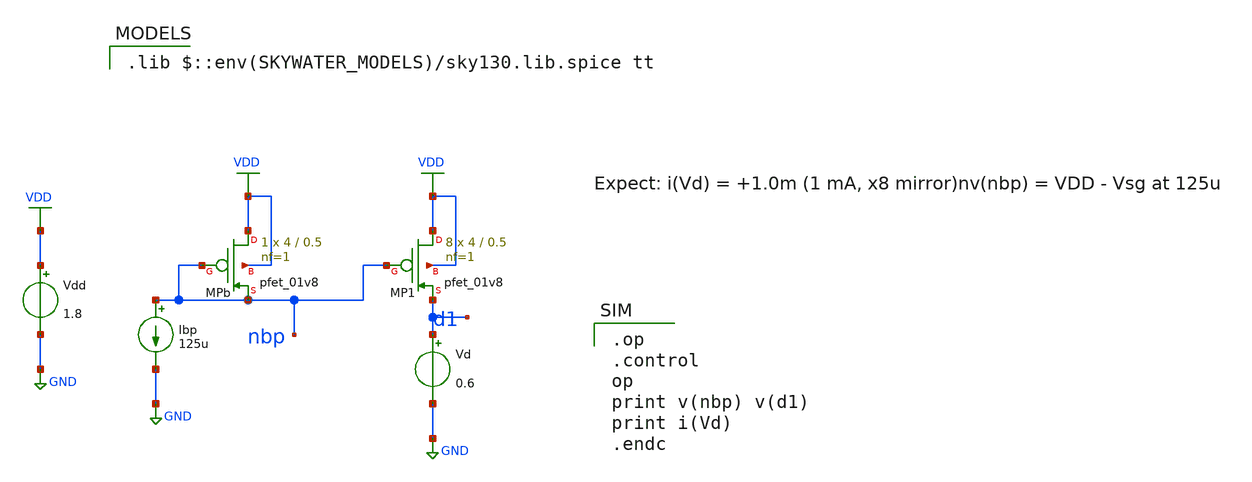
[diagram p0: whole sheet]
** sch_path: 09-sky130-gilbert-mixer-rfic/schematics/2_bleed_bias.sch
**.subckt 2_bleed_bias
XMPb VDD nbp nbp VDD sky130_fd_pr__pfet_01v8 L=0.5 W=4 nf=1 ad='int((nf+1)/2) * W/nf * 0.29' as='int((nf+2)/2) * W/nf * 0.29'
+ pd='2*int((nf+1)/2) * (W/nf + 0.29)' ps='2*int((nf+2)/2) * (W/nf + 0.29)' nrd='0.29 / W' nrs='0.29 / W'
+ sa=0 sb=0 sd=0 mult=1 m=1
Ibp nbp GND 125u
XMP1 VDD nbp d1 VDD sky130_fd_pr__pfet_01v8 L=0.5 W=4 nf=1 ad='int((nf+1)/2) * W/nf * 0.29' as='int((nf+2)/2) * W/nf * 0.29'
+ pd='2*int((nf+1)/2) * (W/nf + 0.29)' ps='2*int((nf+2)/2) * (W/nf + 0.29)' nrd='0.29 / W' nrs='0.29 / W'
+ sa=0 sb=0 sd=0 mult=8 m=8
Vd d1 GND 0.6
Vdd VDD GND 1.8
**** begin user architecture code
 .lib $::env(SKYWATER_MODELS)/sky130.lib.spice tt

.op
.control
op
print v(nbp) v(d1)
print i(Vd)
.endc

**** end user architecture code
**.ends
.GLOBAL VDD
.GLOBAL GND
.end
